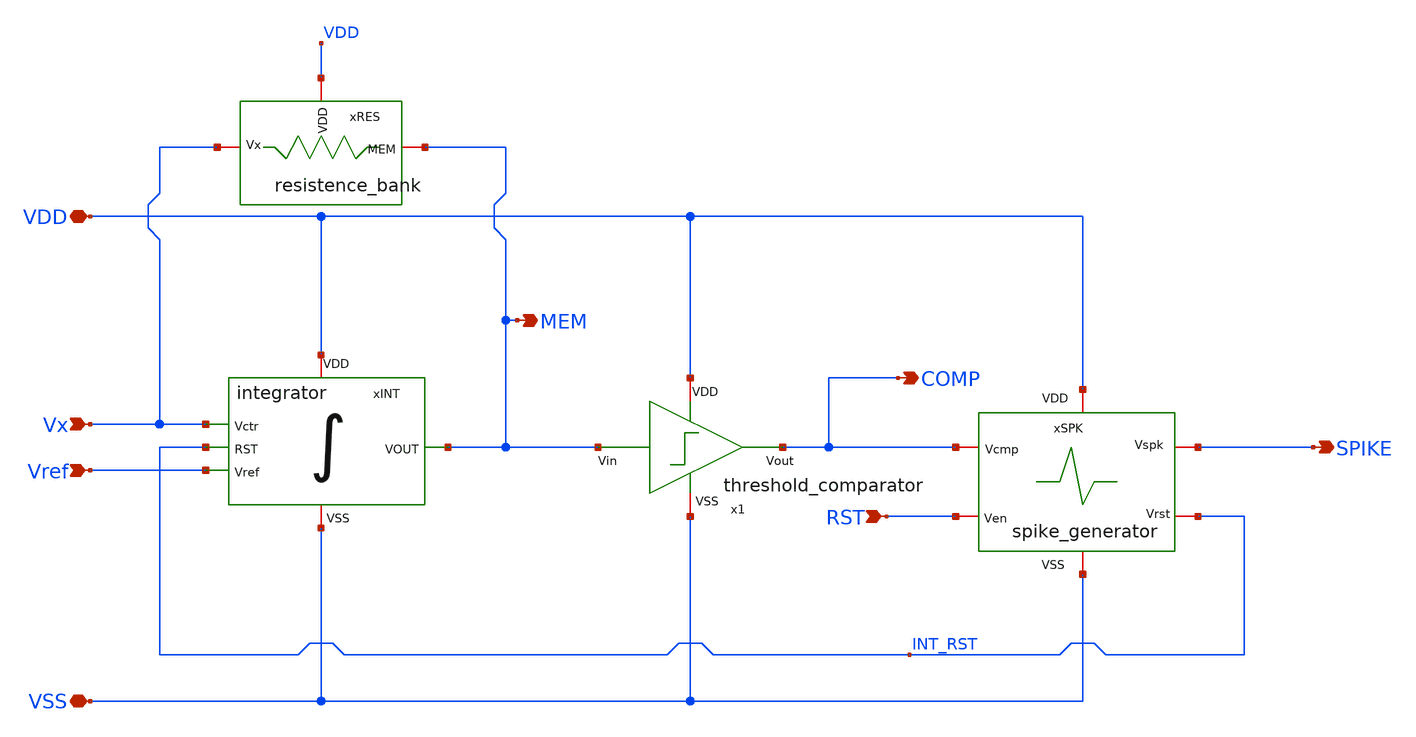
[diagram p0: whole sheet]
** sch_path: work/LIF_neuron/xschem/LIF_neuron.sch
**.subckt LIF_neuron VDD VSS MEM Vx Vref SPIKE RST COMP
*.iopin VDD
*.iopin VSS
*.opin MEM
*.ipin Vx
*.ipin Vref
*.opin SPIKE
*.ipin RST
*.opin COMP
xINT Vref VSS VDD INT_RST Vx MEM integrator
xSPK VDD COMP SPIKE INT_RST RST VSS spike_generator
xRES VDD MEM Vx resistence_bank
x1 VDD MEM COMP VSS threshold_comparator
**.ends
.end
